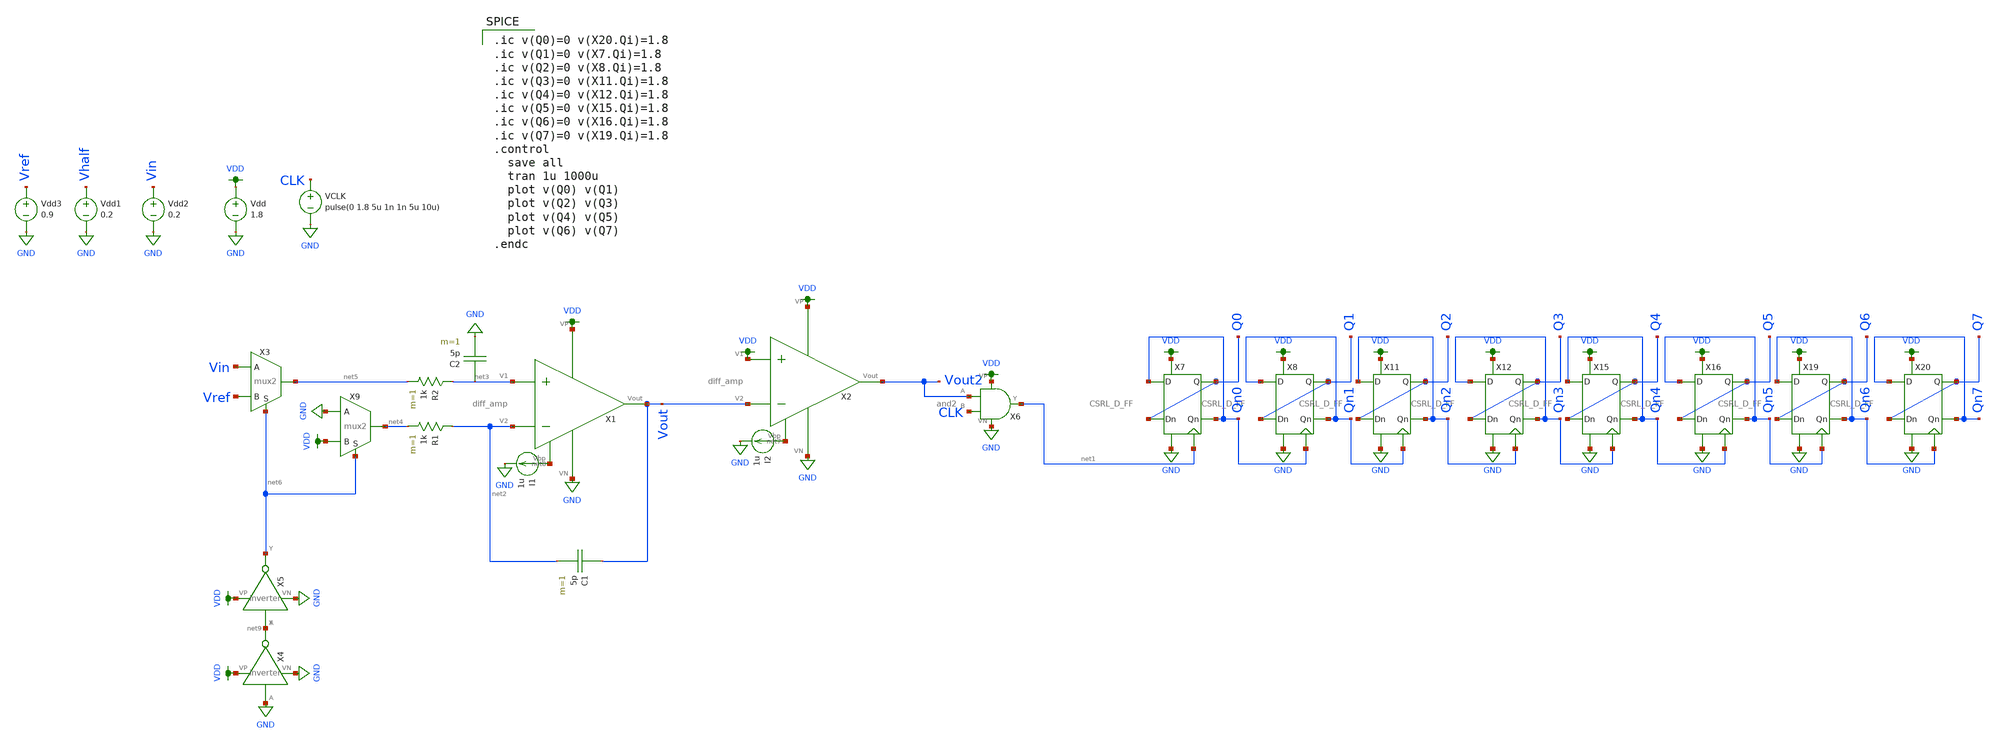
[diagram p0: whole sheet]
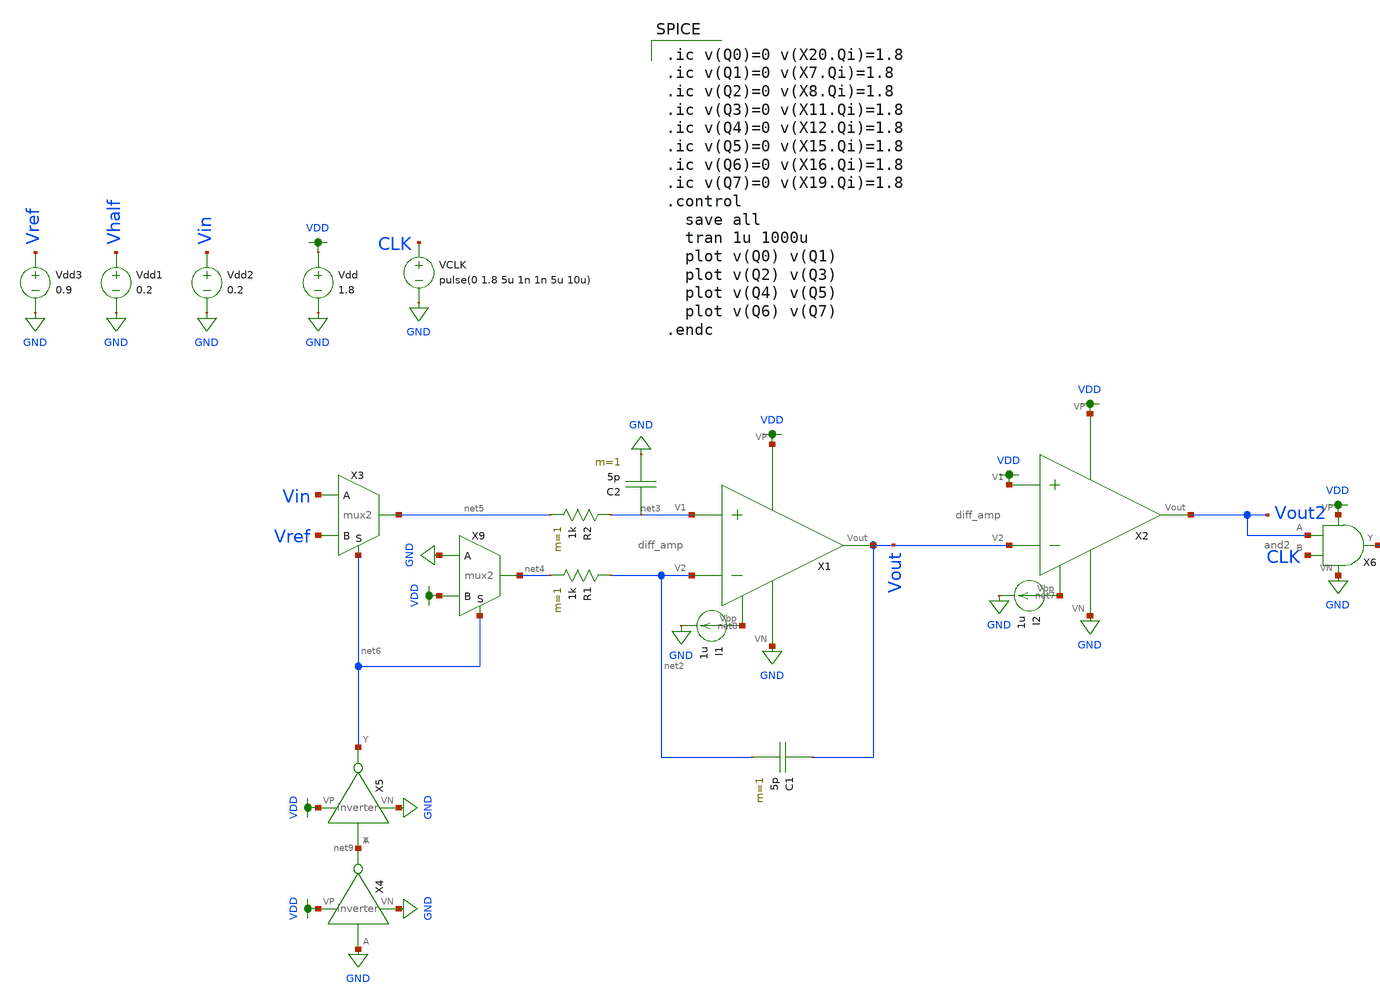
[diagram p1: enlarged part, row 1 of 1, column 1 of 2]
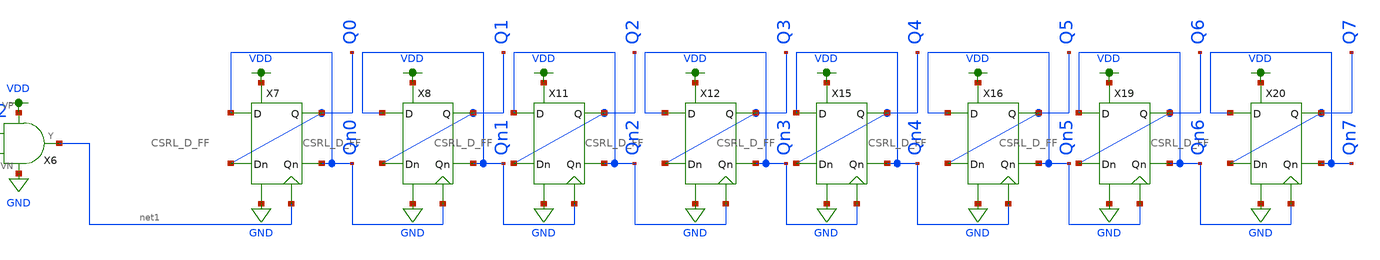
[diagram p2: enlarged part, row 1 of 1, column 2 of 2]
** sch_path: schematic/double-slope-thomas_new.sch
**.subckt double-slope-thomas_new
X2 VDD net7 Vout2 VDD Vout GND diff_amp
Vdd VDD GND 1.8
VCLK CLK GND pulse(0 1.8 5u 1n 1n 5u 10u)
Vdd1 Vhalf GND 0.2
Vdd2 Vin GND 0.2
X7 Q0 Qn0 Qn0 Q0 GND VDD net1 CSRL_D_FF
X8 Q1 Qn1 Qn1 Q1 GND VDD Qn0 CSRL_D_FF
X11 Q2 Qn2 Qn2 Q2 GND VDD Qn1 CSRL_D_FF
X12 Q3 Qn3 Qn3 Q3 GND VDD Qn2 CSRL_D_FF
X15 Q4 Qn4 Qn4 Q4 GND VDD Qn3 CSRL_D_FF
X16 Q5 Qn5 Qn5 Q5 GND VDD Qn4 CSRL_D_FF
X19 Q6 Qn6 Qn6 Q6 GND VDD Qn5 CSRL_D_FF
X20 Q7 Qn7 Qn7 Q7 GND VDD Qn6 CSRL_D_FF
I2 net7 GND 1u
C1 Vout net2 5p m=1
X1 VDD net8 Vout net3 net2 GND diff_amp
R1 net2 net4 1k m=1
C2 net3 GND 5p m=1
R2 net3 net5 1k m=1
I1 net8 GND 1u
X3 net5 Vin Vref net6 mux2
Vdd3 Vref GND 0.9
X4 GND net9 VDD GND inverter
X5 net9 net6 VDD GND inverter
X6 VDD Vout2 GND net1 CLK and2
X9 net4 GND VDD net6 mux2
**** begin user architecture code

.ic v(Q0)=0 v(X20.Qi)=1.8
.ic v(Q1)=0 v(X7.Qi)=1.8
.ic v(Q2)=0 v(X8.Qi)=1.8
.ic v(Q3)=0 v(X11.Qi)=1.8
.ic v(Q4)=0 v(X12.Qi)=1.8
.ic v(Q5)=0 v(X15.Qi)=1.8
.ic v(Q6)=0 v(X16.Qi)=1.8
.ic v(Q7)=0 v(X19.Qi)=1.8
.control
  save all
  tran 1u 1000u
  plot v(Q0) v(Q1)
  plot v(Q2) v(Q3)
  plot v(Q4) v(Q5)
  plot v(Q6) v(Q7)
.endc


.option wnflag=1
.param MC_SWITCH=0.0
.lib ~/skywater/skywater-pdk/libraries/sky130_fd_pr_ngspice/latest/models/sky130.lib.spice tt

**** end user architecture code
**.ends
.GLOBAL GND
.GLOBAL VDD
.end
